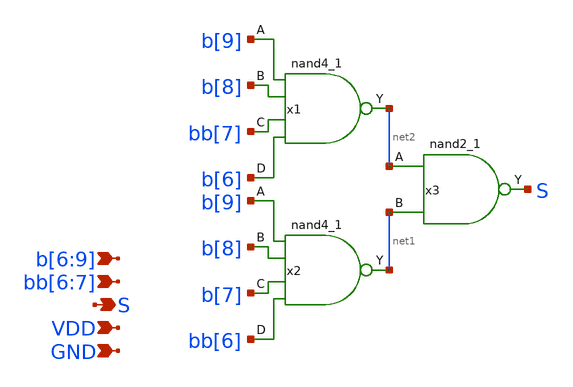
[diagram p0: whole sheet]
** sch_path: xschem/seg_selector_3_logic.sch
**.subckt seg_selector_3_logic S GND VDD b[6],b[7],b[8],b[9] bb[6],bb[7]
*.opin S
*.ipin GND
*.ipin VDD
*.ipin b[6],b[7],b[8],b[9]
*.ipin bb[6],bb[7]
x2 b[9] b[8] b[7] bb[6] GND GND VDD VDD net1 sky130_fd_sc_hd__nand4_1
x1 b[9] b[8] bb[7] b[6] GND GND VDD VDD net2 sky130_fd_sc_hd__nand4_1
x3 net2 net1 GND GND VDD VDD S sky130_fd_sc_hd__nand2_1
**.ends
.end
